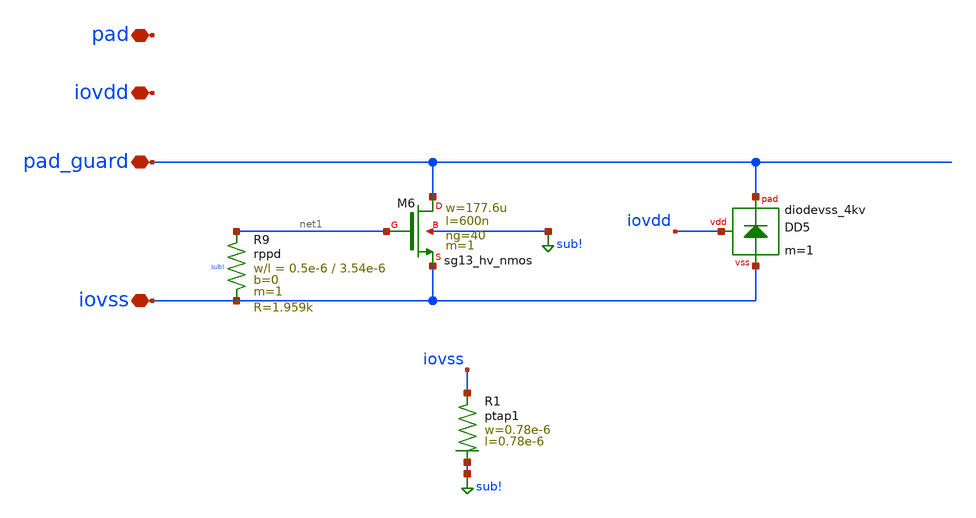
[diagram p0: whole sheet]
** sch_path: trident_test_structures/design_data/xschem/IOPadAnalogGuardLayer/guard_vss_first_stage_esd.sch
**.subckt guard_vss_first_stage_esd iovss pad_guard iovdd pad
*.iopin iovss
*.iopin pad_guard
*.iopin iovdd
*.iopin pad
XM6 pad_guard net1 iovss sub! sg13_hv_nmos w=177.6u l=600n ng=40 m=1 mm_ok=1
XR9 net1 iovss sub! rppd w=0.5e-6 l=3.54e-6 m=1 b=0 mm_ok=1
XR1 iovss sub! ptap1 R=262.8 w=0.78e-6 l=0.78e-6
XD5 iovdd pad_guard iovss diodevss_4kv m=1
**.ends
.GLOBAL sub!
.end
